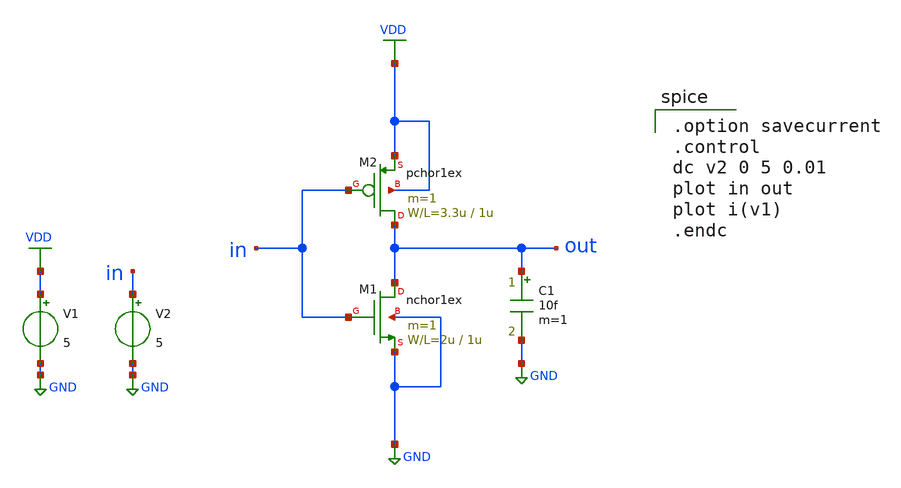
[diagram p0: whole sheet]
** sch_path: member_project/ckdur/inv_tb.sch
**.subckt inv_tb
M1 out in GND GND nchor1ex L=1u W=2u m=1
M2 out in VDD VDD pchor1ex L=1u W=3.3u m=1
V1 VDD GND 5
V2 in GND 5
C1 out GND 10f m=1
**** begin user architecture code
 .include $::LIB/mos.lib
.include $::LIB/passive.lib
.include $::LIB/diode.lib

.option savecurrent
.control
dc v2 0 5 0.01
plot in out
plot i(v1)
.endc


**** end user architecture code
**.ends
.GLOBAL GND
.GLOBAL VDD
.end
